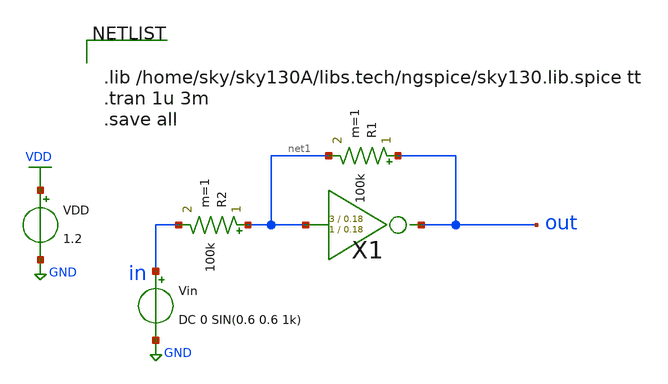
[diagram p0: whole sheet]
** sch_path: xschem/inv/inv_fb_tb.sch
**.subckt inv_fb_tb
Vin in GND DC 0 SIN(0.6 0.6 1k)
VDD VDD GND 1.2
X1 net1 out inv Wpmos=3 Lpmos=0.18 Wnmos=1 Lnmos=0.18
R1 out net1 100k m=1
R2 net1 in 100k m=1
**** begin user architecture code


.lib /home/sky/sky130A/libs.tech/ngspice/sky130.lib.spice tt
.tran 1u 3m
.save all


**** end user architecture code
**.ends

* expanding   symbol:  inv/inv.sym # of pins=2
** sym_path: xschem/inv/inv.sym
** sch_path: xschem/inv/inv.sch
.subckt inv in out  Wpmos=3 Lpmos=0.18 Wnmos=1 Lnmos=0.18
*.ipin in
*.iopin out
XM1 out in GND GND sky130_fd_pr__nfet_01v8 L=Lnmos W=Wnmos nf=1 ad='int((nf+1)/2) * W/nf * 0.29' as='int((nf+2)/2) * W/nf * 0.29'
+ pd='2*int((nf+1)/2) * (W/nf + 0.29)' ps='2*int((nf+2)/2) * (W/nf + 0.29)' nrd='0.29 / W' nrs='0.29 / W'
+ sa=0 sb=0 sd=0 mult=1 m=1
XM2 out in VDD VDD sky130_fd_pr__pfet_01v8 L=Lpmos W=Wpmos nf=1 ad='int((nf+1)/2) * W/nf * 0.29' as='int((nf+2)/2) * W/nf * 0.29'
+ pd='2*int((nf+1)/2) * (W/nf + 0.29)' ps='2*int((nf+2)/2) * (W/nf + 0.29)' nrd='0.29 / W' nrs='0.29 / W'
+ sa=0 sb=0 sd=0 mult=1 m=1
.ends

.GLOBAL VDD
.GLOBAL GND
.end
